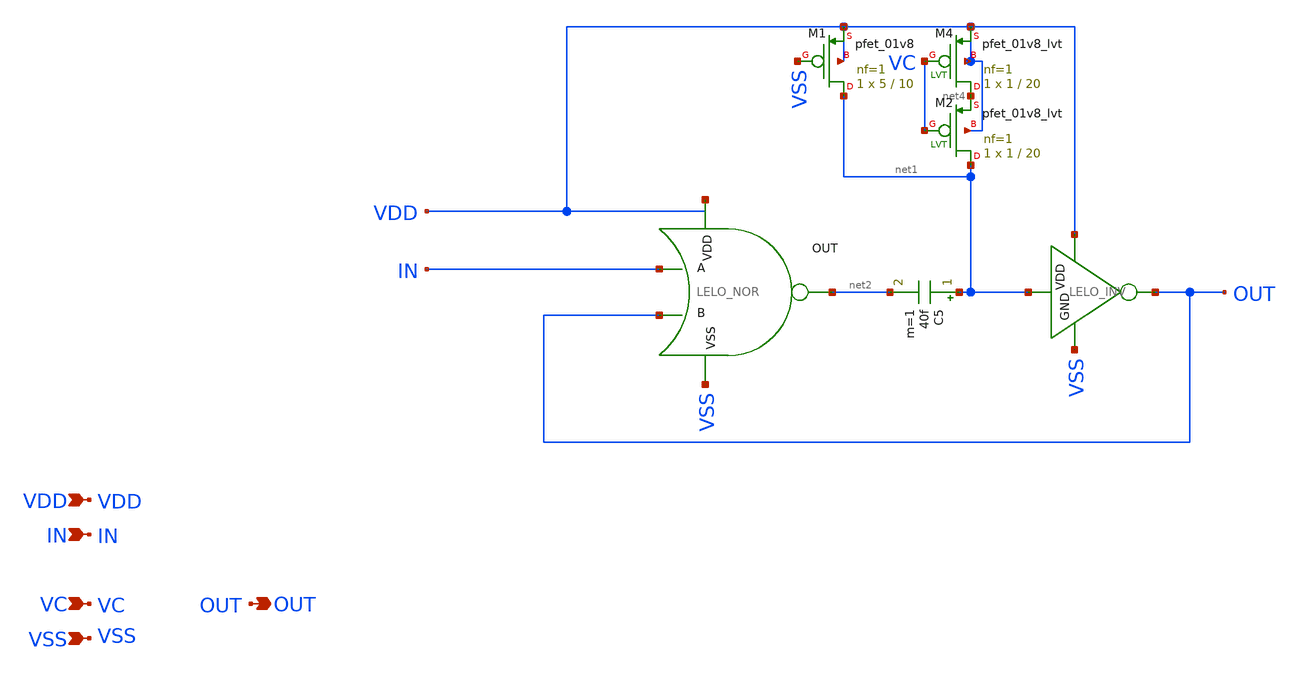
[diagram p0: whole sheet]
** sch_path: design/LELO_SVOD_SKY130A/LELO_ONESHOT_VC.sch
**.subckt LELO_ONESHOT_VC VDD IN VC VSS OUT
*.ipin VDD
*.ipin IN
*.ipin VC
*.ipin VSS
*.opin OUT
x2 net3 net2 IN OUT VSS LELO_NOR
C5 net1 net2 40f m=1
x3 VDD net1 OUT VSS LELO_INV
XM4 net4 VC VDD VDD sky130_fd_pr__pfet_01v8_lvt L=20 W=1 nf=1 ad='int((1 + 1)/2) * 1 / 1 * 0.29' as='int((1 + 2)/2) * 1 / 1 * 0.29'
+ pd='2*int((1 + 1)/2) * (1 / 1 + 0.29)' ps='2*int((1 + 2)/2) * (1 / 1 + 0.29)' nrd='0.29 / 1 ' nrs='0.29 / 1 '
+ sa=0 sb=0 sd=0 mult=1 m=1
XM1 net1 VSS VDD VDD sky130_fd_pr__pfet_01v8 L=10 W=5 nf=1 ad='int((1 + 1)/2) * 5 / 1 * 0.29' as='int((1 + 2)/2) * 5 / 1 * 0.29'
+ pd='2*int((1 + 1)/2) * (5 / 1 + 0.29)' ps='2*int((1 + 2)/2) * (5 / 1 + 0.29)' nrd='0.29 / 5 ' nrs='0.29 / 5 '
+ sa=0 sb=0 sd=0 mult=1 m=1
XM2 net1 VC net4 VDD sky130_fd_pr__pfet_01v8_lvt L=20 W=1 nf=1 ad='int((1 + 1)/2) * 1 / 1 * 0.29' as='int((1 + 2)/2) * 1 / 1 * 0.29'
+ pd='2*int((1 + 1)/2) * (1 / 1 + 0.29)' ps='2*int((1 + 2)/2) * (1 / 1 + 0.29)' nrd='0.29 / 1 ' nrs='0.29 / 1 '
+ sa=0 sb=0 sd=0 mult=1 m=1
**.ends

* expanding   symbol:  LELO_SVOD_SKY130A/LELO_NOR.sym # of pins=5
** sym_path: design/LELO_SVOD_SKY130A/LELO_NOR.sym
** sch_path: design/LELO_SVOD_SKY130A/LELO_NOR.sch
.subckt LELO_NOR VDD OUT A B VSS
*.ipin VDD
*.ipin VSS
*.opin OUT
*.ipin A
*.ipin B
XM2 OUT B VSS VSS sky130_fd_pr__nfet_01v8 L=0.15 W=2 nf=1 ad='int((1 + 1)/2) * 2 / 1 * 0.29' as='int((1 + 2)/2) * 2 / 1 * 0.29'
+ pd='2*int((1 + 1)/2) * (2 / 1 + 0.29)' ps='2*int((1 + 2)/2) * (2 / 1 + 0.29)' nrd='0.29 / 2 ' nrs='0.29 / 2 '
+ sa=0 sb=0 sd=0 mult=1 m=1
XM1 OUT A VSS VSS sky130_fd_pr__nfet_01v8 L=0.15 W=2 nf=1 ad='int((1 + 1)/2) * 2 / 1 * 0.29' as='int((1 + 2)/2) * 2 / 1 * 0.29'
+ pd='2*int((1 + 1)/2) * (2 / 1 + 0.29)' ps='2*int((1 + 2)/2) * (2 / 1 + 0.29)' nrd='0.29 / 2 ' nrs='0.29 / 2 '
+ sa=0 sb=0 sd=0 mult=1 m=1
XM3 OUT B net1 VDD sky130_fd_pr__pfet_01v8 L=0.15 W=4 nf=1 ad='int((1 + 1)/2) * 4 / 1 * 0.29' as='int((1 + 2)/2) * 4 / 1 * 0.29'
+ pd='2*int((1 + 1)/2) * (4 / 1 + 0.29)' ps='2*int((1 + 2)/2) * (4 / 1 + 0.29)' nrd='0.29 / 4 ' nrs='0.29 / 4 '
+ sa=0 sb=0 sd=0 mult=1 m=1
XM4 net1 A VDD VDD sky130_fd_pr__pfet_01v8 L=0.15 W=4 nf=1 ad='int((1 + 1)/2) * 4 / 1 * 0.29' as='int((1 + 2)/2) * 4 / 1 * 0.29'
+ pd='2*int((1 + 1)/2) * (4 / 1 + 0.29)' ps='2*int((1 + 2)/2) * (4 / 1 + 0.29)' nrd='0.29 / 4 ' nrs='0.29 / 4 '
+ sa=0 sb=0 sd=0 mult=1 m=1
.ends


* expanding   symbol:  LELO_SVOD_SKY130A/LELO_INV.sym # of pins=4
** sym_path: design/LELO_SVOD_SKY130A/LELO_INV.sym
** sch_path: design/LELO_SVOD_SKY130A/LELO_INV.sch
.subckt LELO_INV VDD VIN VOUT GND
*.ipin VIN
*.ipin VDD
*.ipin GND
*.opin VOUT
XM1 VOUT VIN GND GND sky130_fd_pr__nfet_01v8_lvt L=0.15 W=1 nf=1 ad='int((1 + 1)/2) * 1 / 1 * 0.29' as='int((1 + 2)/2) * 1 / 1 * 0.29'
+ pd='2*int((1 + 1)/2) * (1 / 1 + 0.29)' ps='2*int((1 + 2)/2) * (1 / 1 + 0.29)' nrd='0.29 / 1 ' nrs='0.29 / 1 '
+ sa=0 sb=0 sd=0 mult=1 m=1
XM2 VOUT VIN VDD VDD sky130_fd_pr__pfet_01v8_lvt L=0.35 W=1 nf=1 ad='int((1 + 1)/2) * 1 / 1 * 0.29' as='int((1 + 2)/2) * 1 / 1 * 0.29'
+ pd='2*int((1 + 1)/2) * (1 / 1 + 0.29)' ps='2*int((1 + 2)/2) * (1 / 1 + 0.29)' nrd='0.29 / 1 ' nrs='0.29 / 1 '
+ sa=0 sb=0 sd=0 mult=2 m=2
.ends

.end
